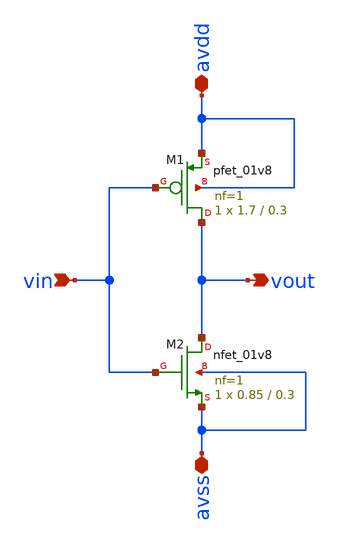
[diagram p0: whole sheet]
** sch_path: XSCHEM_DESIGNS/Inverter.sch
**.subckt Inverter vin vout avdd avss
*.ipin vin
*.opin vout
*.iopin avdd
*.iopin avss
XM1 vout vin avdd avdd sky130_fd_pr__pfet_01v8 L=0.3 W=1.7 nf=1 ad='int((1 + 1)/2) * 1.7 / 1 * 0.29'
+ as='int((1 + 2)/2) * 1.7 / 1 * 0.29' pd='2*int((1 + 1)/2) * (1.7 / 1 + 0.29)' ps='2*int((1 + 2)/2) * (1.7 / 1 + 0.29)'
+ nrd='0.29 / 1.7 ' nrs='0.29 / 1.7 ' sa=0 sb=0 sd=0 mult=1 m=1
XM2 vout vin avss avss sky130_fd_pr__nfet_01v8 L=0.3 W=0.85 nf=1 ad='int((1 + 1)/2) * 0.85 / 1 * 0.29'
+ as='int((1 + 2)/2) * 0.85 / 1 * 0.29' pd='2*int((1 + 1)/2) * (0.85 / 1 + 0.29)' ps='2*int((1 + 2)/2) * (0.85 / 1 + 0.29)'
+ nrd='0.29 / 0.85 ' nrs='0.29 / 0.85 ' sa=0 sb=0 sd=0 mult=1 m=1
**.ends
.end
